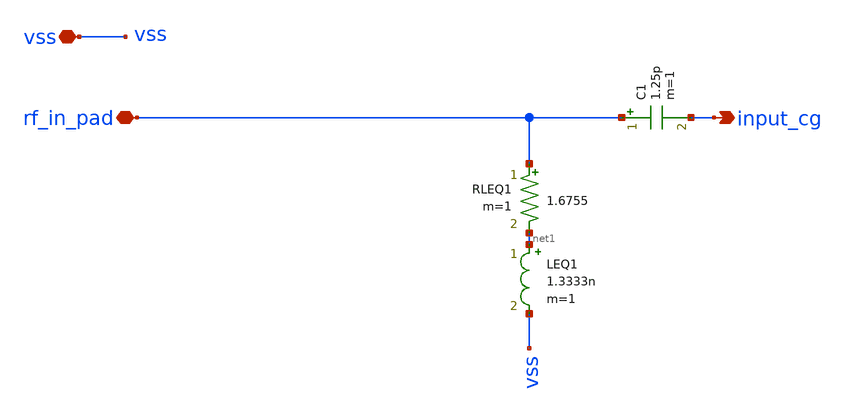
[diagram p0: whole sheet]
** sch_path: xschem/lna_core_input_match.sch
**.subckt lna_core_input_match rf_in_pad vss input_cg
*.iopin rf_in_pad
*.iopin vss
*.opin input_cg
LEQ1 net1 vss 1.3333n m=1
C1 rf_in_pad input_cg 1.25p m=1
RLEQ1 rf_in_pad net1 1.6755 m=1
**.ends
.end
